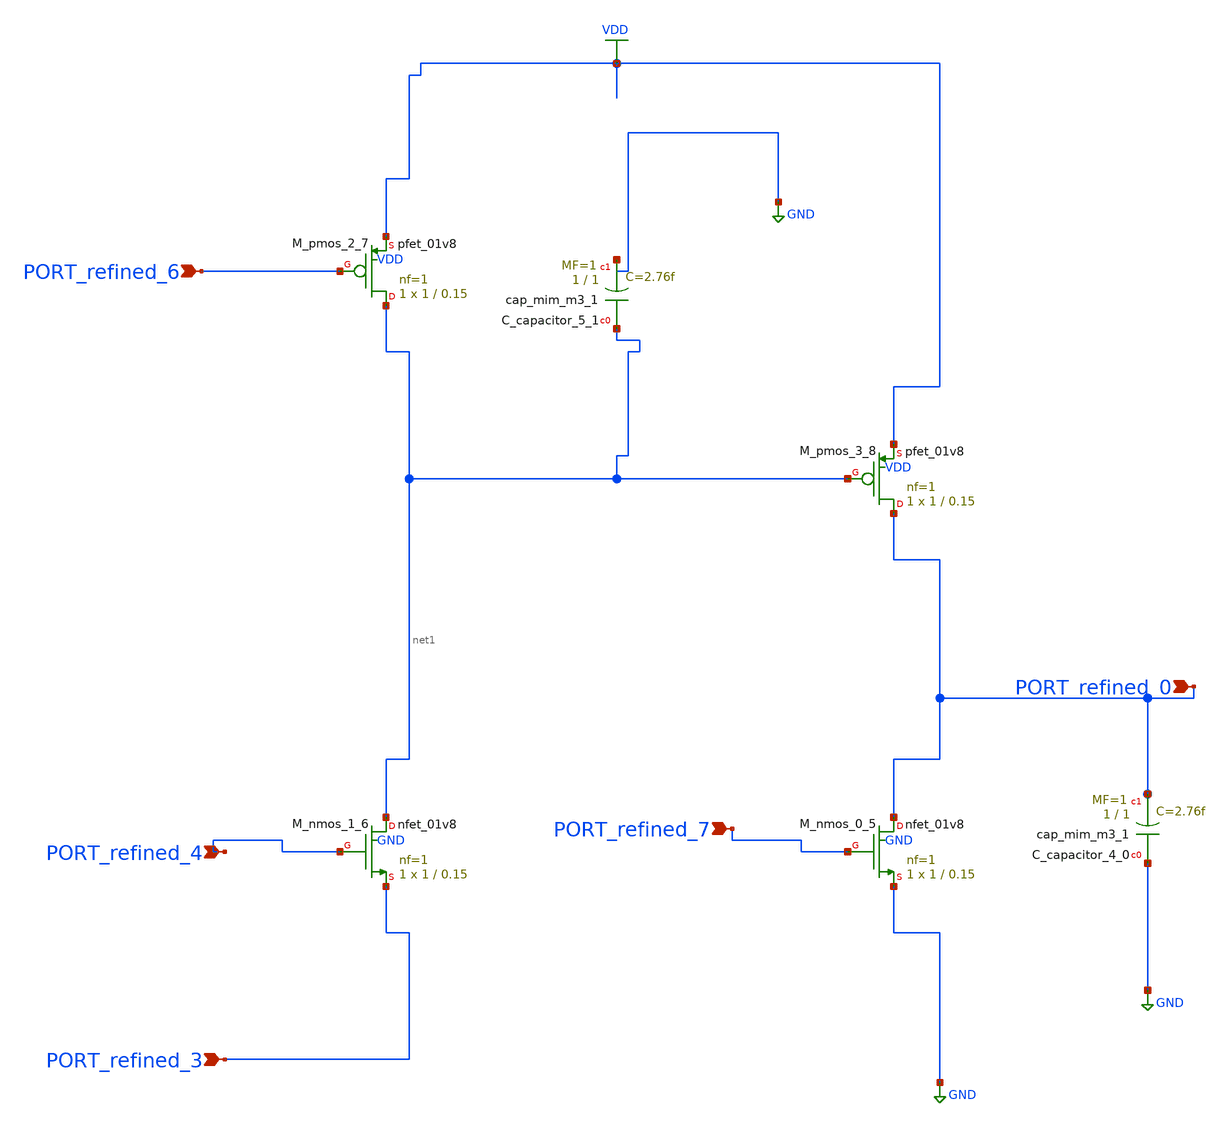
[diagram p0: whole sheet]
** sch_path: schematics/10_1007_s00034-017-0630-6_05_001_crop1.sch
**.subckt 10_1007_s00034-017-0630-6_05_001_crop1 PORT_refined_3 PORT_refined_0 PORT_refined_7
*+ PORT_refined_4 PORT_refined_6
*.ipin PORT_refined_3
*.ipin PORT_refined_0
*.ipin PORT_refined_7
*.ipin PORT_refined_4
*.ipin PORT_refined_6
XC_capacitor_4_0 GND PORT_refined_0 sky130_fd_pr__cap_mim_m3_1 W=1 L=1 MF=1 m=1
XC_capacitor_5_1 net1 GND sky130_fd_pr__cap_mim_m3_1 W=1 L=1 MF=1 m=1
XM_nmos_0_5 PORT_refined_0 PORT_refined_7 GND GND sky130_fd_pr__nfet_01v8 L=0.15 W=1 nf=1 ad='int((1 + 1)/2) * 1 / 1 * 0.29'
+ as='int((1 + 2)/2) * 1 / 1 * 0.29' pd='2*int((1 + 1)/2) * (1 / 1 + 0.29)' ps='2*int((1 + 2)/2) * (1 / 1 + 0.29)'
+ nrd='0.29 / 1 ' nrs='0.29 / 1 ' sa=0 sb=0 sd=0 mult=1 m=1
XM_nmos_1_6 net1 PORT_refined_4 PORT_refined_3 GND sky130_fd_pr__nfet_01v8 L=0.15 W=1 nf=1 ad='int((1 + 1)/2) * 1 / 1 * 0.29'
+ as='int((1 + 2)/2) * 1 / 1 * 0.29' pd='2*int((1 + 1)/2) * (1 / 1 + 0.29)' ps='2*int((1 + 2)/2) * (1 / 1 + 0.29)'
+ nrd='0.29 / 1 ' nrs='0.29 / 1 ' sa=0 sb=0 sd=0 mult=1 m=1
XM_pmos_2_7 net1 PORT_refined_6 VDD VDD sky130_fd_pr__pfet_01v8 L=0.15 W=1 nf=1 ad='int((1 + 1)/2) * 1 / 1 * 0.29'
+ as='int((1 + 2)/2) * 1 / 1 * 0.29' pd='2*int((1 + 1)/2) * (1 / 1 + 0.29)' ps='2*int((1 + 2)/2) * (1 / 1 + 0.29)'
+ nrd='0.29 / 1 ' nrs='0.29 / 1 ' sa=0 sb=0 sd=0 mult=1 m=1
XM_pmos_3_8 PORT_refined_0 net1 VDD VDD sky130_fd_pr__pfet_01v8 L=0.15 W=1 nf=1 ad='int((1 + 1)/2) * 1 / 1 * 0.29'
+ as='int((1 + 2)/2) * 1 / 1 * 0.29' pd='2*int((1 + 1)/2) * (1 / 1 + 0.29)' ps='2*int((1 + 2)/2) * (1 / 1 + 0.29)'
+ nrd='0.29 / 1 ' nrs='0.29 / 1 ' sa=0 sb=0 sd=0 mult=1 m=1
**.ends
.GLOBAL GND
.GLOBAL VDD
.end
